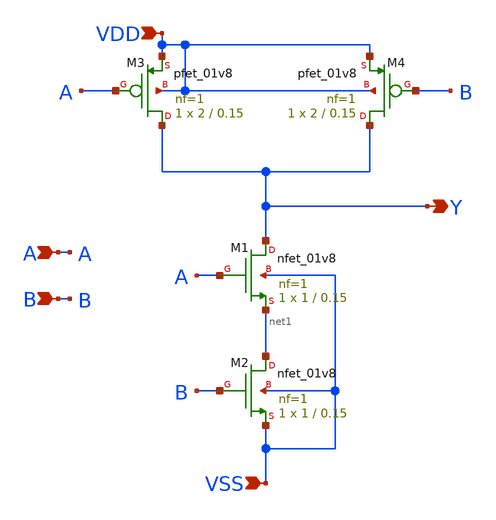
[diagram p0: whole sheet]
** sch_path: nand_FFD.sch
**.subckt nand_FFD VDD A B VSS Y
*.ipin VDD
*.ipin A
*.ipin B
*.ipin VSS
*.opin Y
XM1 Y A net1 VSS sky130_fd_pr__nfet_01v8 L=0.15 W=1 nf=1 ad='int((nf+1)/2) * W/nf * 0.29' as='int((nf+2)/2) * W/nf * 0.29'
+ pd='2*int((nf+1)/2) * (W/nf + 0.29)' ps='2*int((nf+2)/2) * (W/nf + 0.29)' nrd='0.29 / W' nrs='0.29 / W'
+ sa=0 sb=0 sd=0 mult=1 m=1
XM2 net1 B VSS VSS sky130_fd_pr__nfet_01v8 L=0.15 W=1 nf=1 ad='int((nf+1)/2) * W/nf * 0.29' as='int((nf+2)/2) * W/nf * 0.29'
+ pd='2*int((nf+1)/2) * (W/nf + 0.29)' ps='2*int((nf+2)/2) * (W/nf + 0.29)' nrd='0.29 / W' nrs='0.29 / W'
+ sa=0 sb=0 sd=0 mult=1 m=1
XM3 Y A VDD VDD sky130_fd_pr__pfet_01v8 L=0.15 W=2 nf=1 ad='int((nf+1)/2) * W/nf * 0.29' as='int((nf+2)/2) * W/nf * 0.29'
+ pd='2*int((nf+1)/2) * (W/nf + 0.29)' ps='2*int((nf+2)/2) * (W/nf + 0.29)' nrd='0.29 / W' nrs='0.29 / W'
+ sa=0 sb=0 sd=0 mult=1 m=1
XM4 Y B VDD VDD sky130_fd_pr__pfet_01v8 L=0.15 W=2 nf=1 ad='int((nf+1)/2) * W/nf * 0.29' as='int((nf+2)/2) * W/nf * 0.29'
+ pd='2*int((nf+1)/2) * (W/nf + 0.29)' ps='2*int((nf+2)/2) * (W/nf + 0.29)' nrd='0.29 / W' nrs='0.29 / W'
+ sa=0 sb=0 sd=0 mult=1 m=1
**.ends
.end
